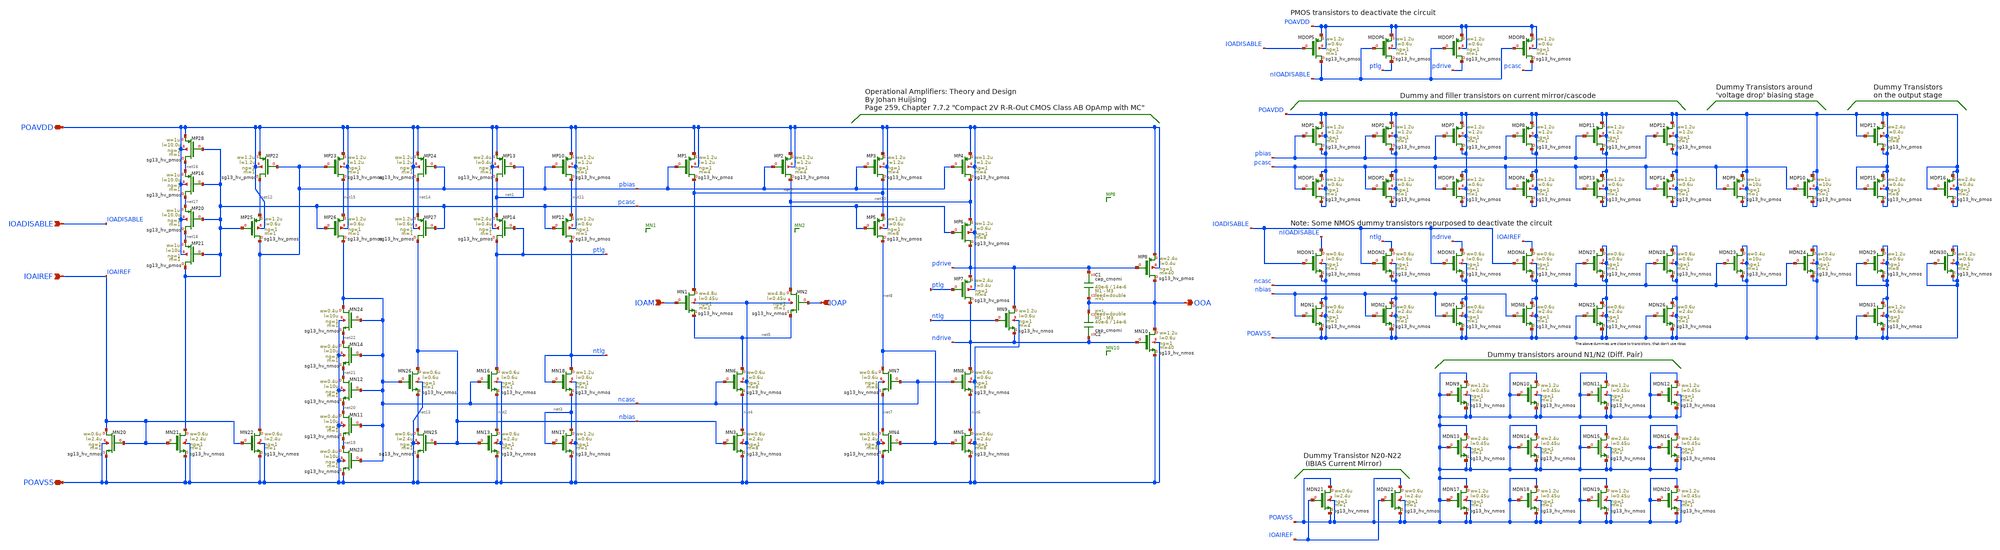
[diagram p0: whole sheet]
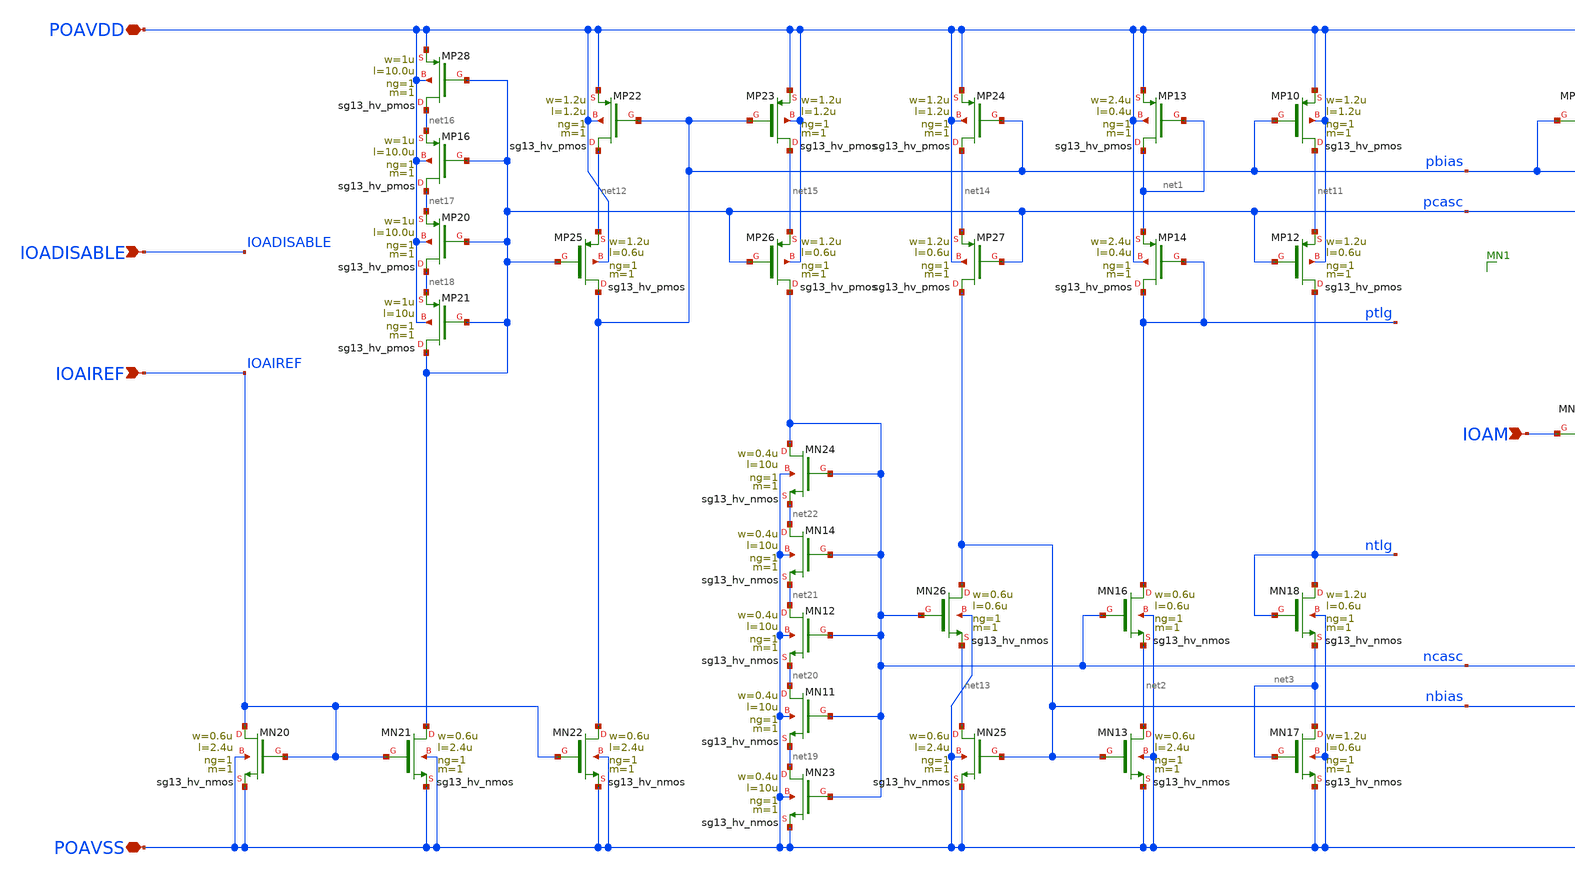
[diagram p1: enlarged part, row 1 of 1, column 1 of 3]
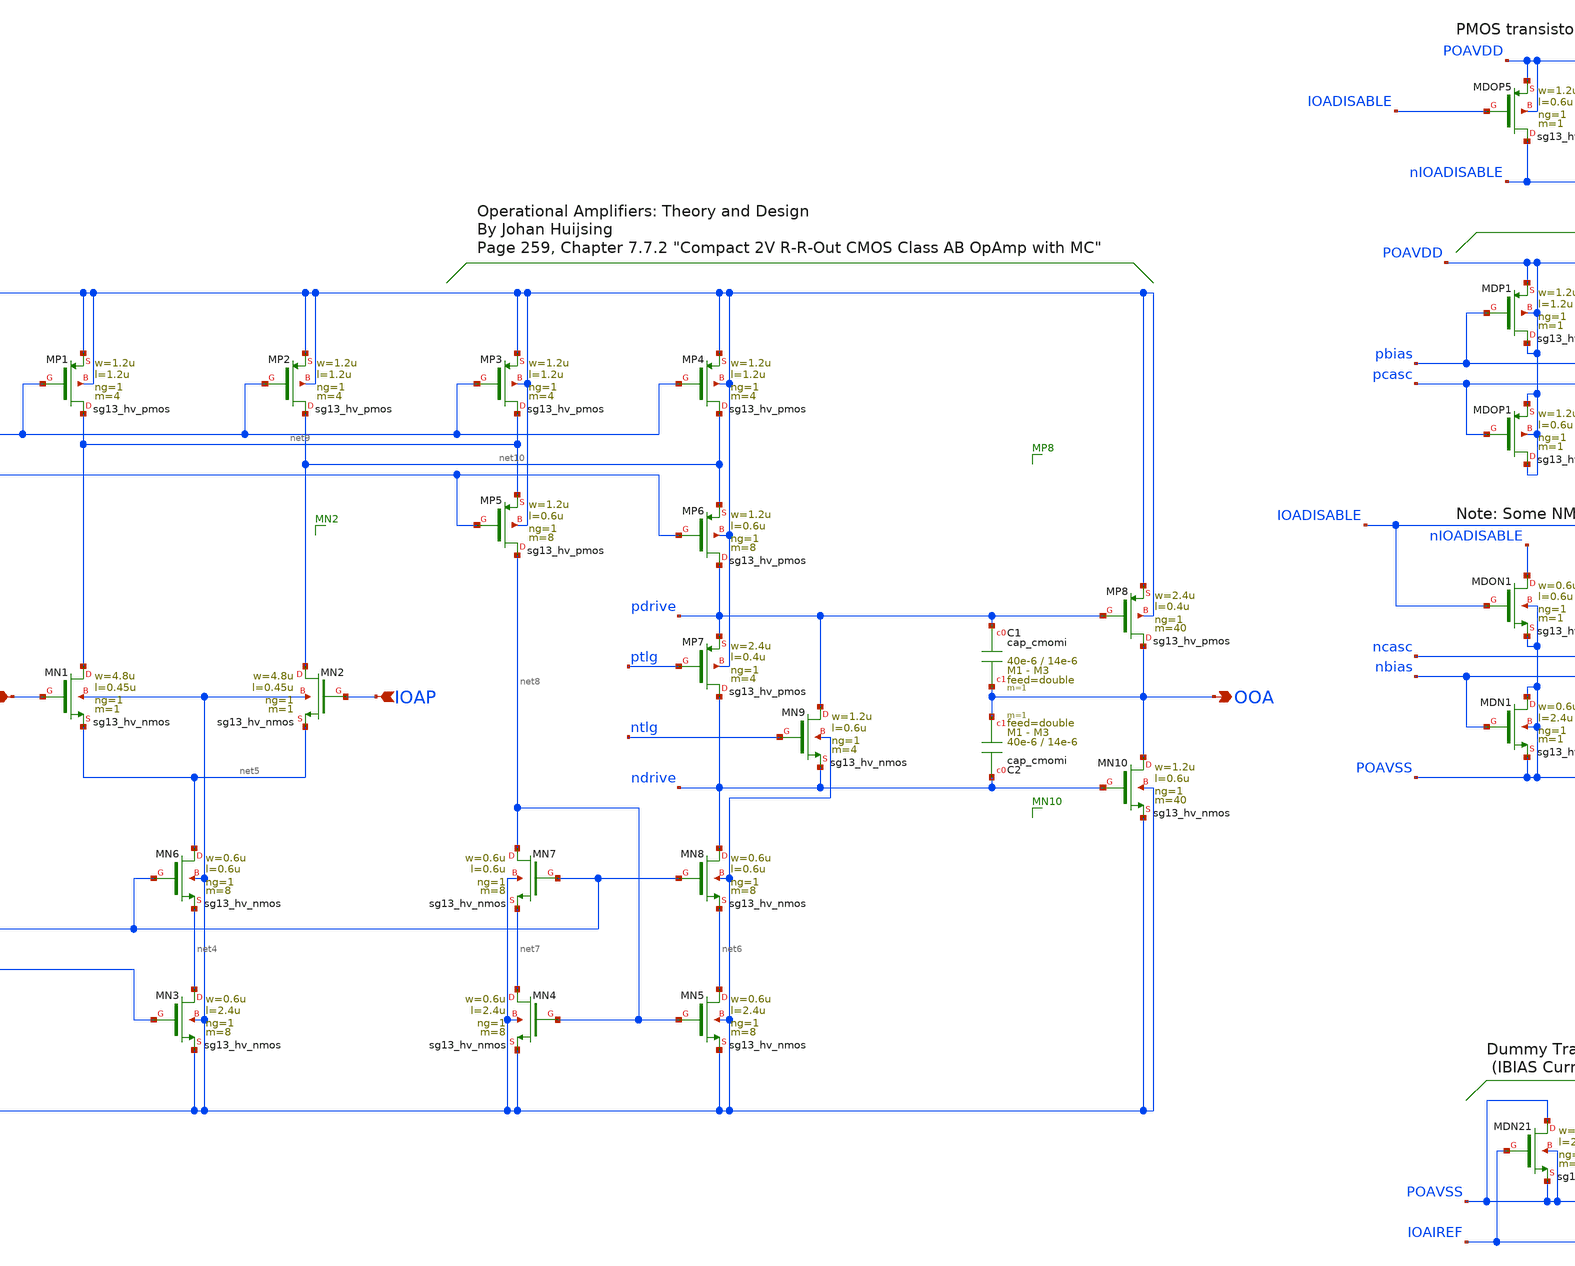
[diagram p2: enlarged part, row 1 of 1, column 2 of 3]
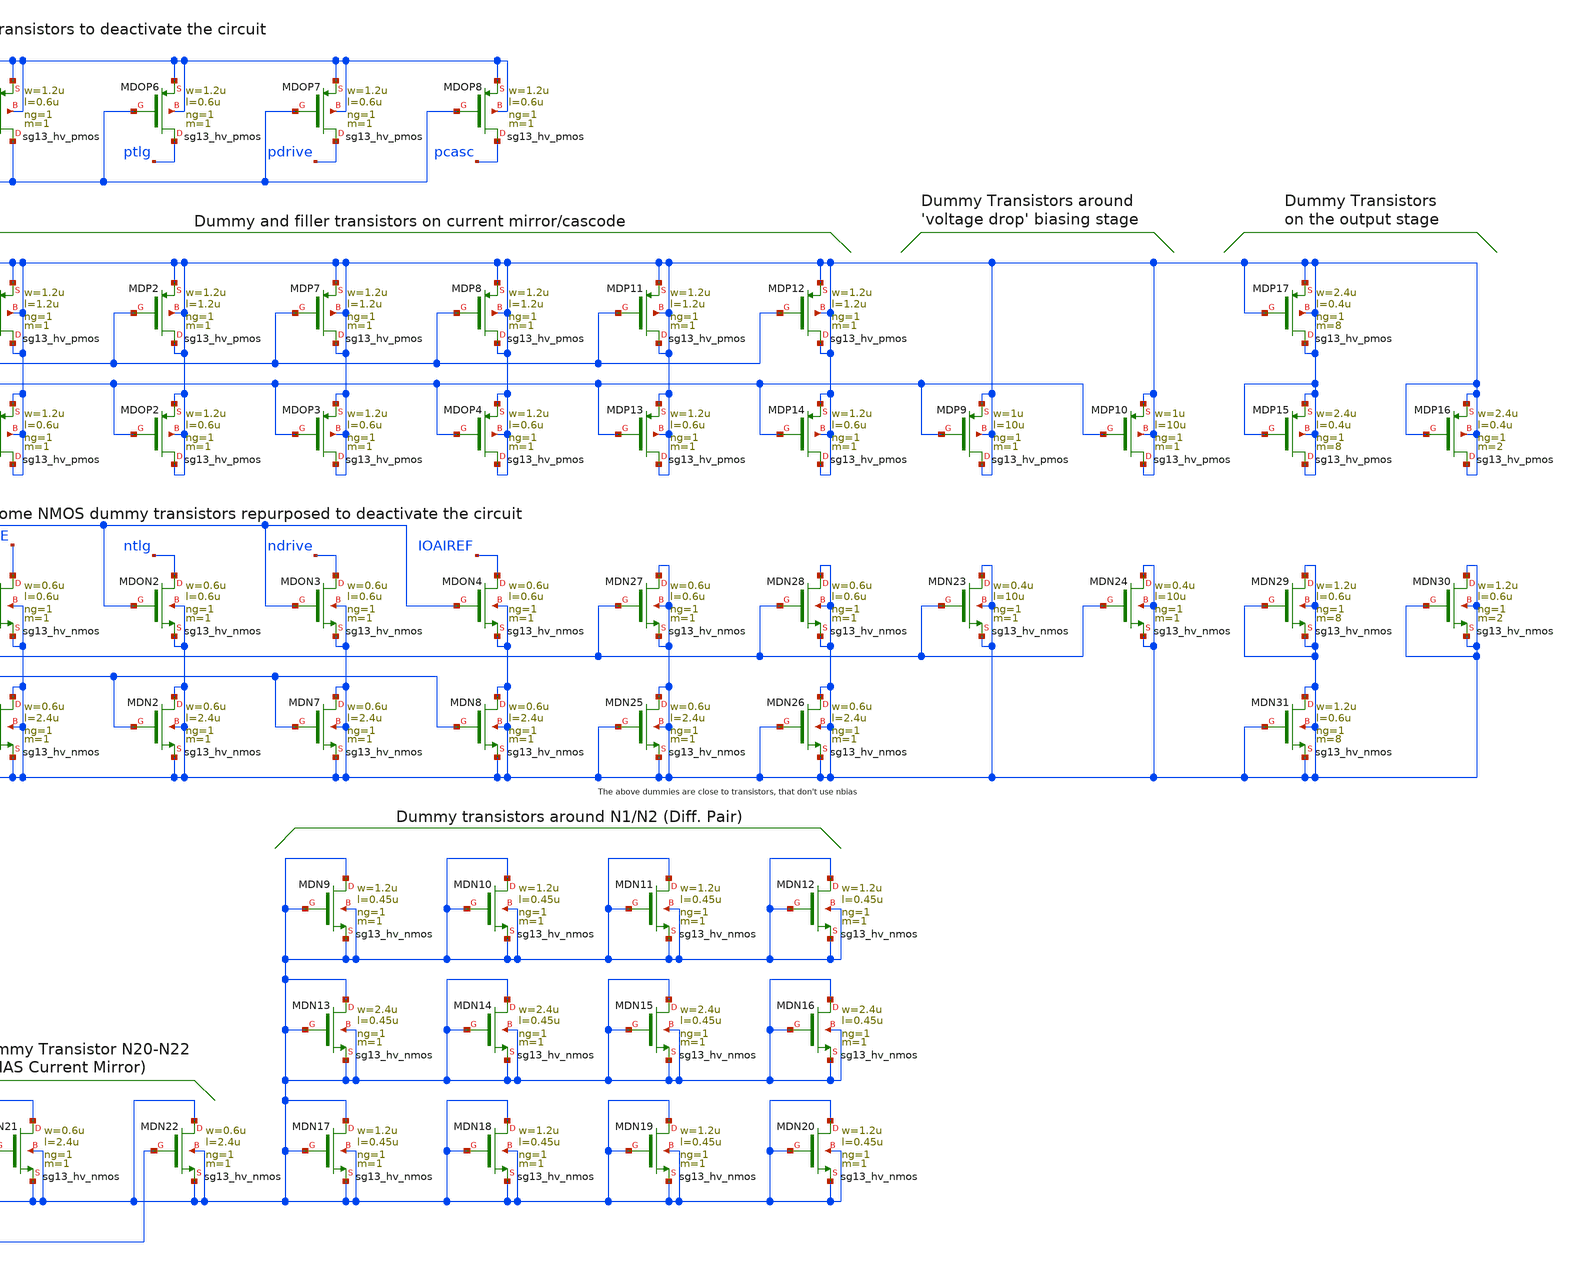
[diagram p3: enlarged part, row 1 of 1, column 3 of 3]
** sch_path: macros/heichips26_FAIf/macros/opamp/schematic/xschem/op_amp_ver_2.sch
**.subckt op_amp_ver_2 POAVDD IOAM IOAP OOA IOAIREF POAVSS IOADISABLE
*.iopin POAVDD
*.ipin IOAM
*.ipin IOAP
*.opin OOA
*.ipin IOAIREF
*.iopin POAVSS
*.ipin IOADISABLE
XMP13 net1 net1 POAVDD POAVDD sg13_hv_pmos w=2.4u l=0.4u ng=1 m=1 mm_ok=1
XMP14 ptlg ptlg net1 POAVDD sg13_hv_pmos w=2.4u l=0.4u ng=1 m=1 mm_ok=1
XMN16 ptlg ncasc net2 POAVSS sg13_hv_nmos w=0.6u l=0.6u ng=1 m=1 mm_ok=1
XMN13 net2 nbias POAVSS POAVSS sg13_hv_nmos w=0.6u l=2.4u ng=1 m=1 mm_ok=1
XMN18 ntlg ntlg net3 POAVSS sg13_hv_nmos w=1.2u l=0.6u ng=1 m=1 mm_ok=1
XMN17 net3 net3 POAVSS POAVSS sg13_hv_nmos w=1.2u l=0.6u ng=1 m=1 mm_ok=1
XMP10 net11 pbias POAVDD POAVDD sg13_hv_pmos w=1.2u l=1.2u ng=1 m=1 mm_ok=1
XMP12 ntlg pcasc net11 POAVDD sg13_hv_pmos w=1.2u l=0.6u ng=1 m=1 mm_ok=1
XMP1 net9 pbias POAVDD POAVDD sg13_hv_pmos w=1.2u l=1.2u ng=1 m=4 mm_ok=1
XMP2 net10 pbias POAVDD POAVDD sg13_hv_pmos w=1.2u l=1.2u ng=1 m=4 mm_ok=1
XMN1 net9 IOAM net5 POAVSS sg13_hv_nmos w=4.8u l=0.45u ng=1 m=1 mm_ok=1
XMN2 net10 IOAP net5 POAVSS sg13_hv_nmos w=4.8u l=0.45u ng=1 m=1 mm_ok=1
XMN3 net4 nbias POAVSS POAVSS sg13_hv_nmos w=0.6u l=2.4u ng=1 m=8 mm_ok=1
XMN6 net5 ncasc net4 POAVSS sg13_hv_nmos w=0.6u l=0.6u ng=1 m=8 mm_ok=1
XMN7 net8 ncasc net7 POAVSS sg13_hv_nmos w=0.6u l=0.6u ng=1 m=8 mm_ok=1
XMN8 ndrive ncasc net6 POAVSS sg13_hv_nmos w=0.6u l=0.6u ng=1 m=8 mm_ok=1
XMN4 net7 net8 POAVSS POAVSS sg13_hv_nmos w=0.6u l=2.4u ng=1 m=8 mm_ok=1
XMN5 net6 net8 POAVSS POAVSS sg13_hv_nmos w=0.6u l=2.4u ng=1 m=8 mm_ok=1
XMP3 net9 pbias POAVDD POAVDD sg13_hv_pmos w=1.2u l=1.2u ng=1 m=4 mm_ok=1
XMP5 net8 pcasc net9 POAVDD sg13_hv_pmos w=1.2u l=0.6u ng=1 m=8 mm_ok=1
XMP4 net10 pbias POAVDD POAVDD sg13_hv_pmos w=1.2u l=1.2u ng=1 m=4 mm_ok=1
XMP6 pdrive pcasc net10 POAVDD sg13_hv_pmos w=1.2u l=0.6u ng=1 m=8 mm_ok=1
XMP7 ndrive ptlg pdrive POAVDD sg13_hv_pmos w=2.4u l=0.4u ng=1 m=4 mm_ok=1
XMN9 pdrive ntlg ndrive POAVSS sg13_hv_nmos w=1.2u l=0.6u ng=1 m=4 mm_ok=1
XMP8 OOA pdrive POAVDD POAVDD sg13_hv_pmos w=2.4u l=0.4u ng=1 m=40 mm_ok=1
XMN10 OOA ndrive POAVSS POAVSS sg13_hv_nmos w=1.2u l=0.6u ng=1 m=40 mm_ok=1
XMN20 IOAIREF IOAIREF POAVSS POAVSS sg13_hv_nmos w=0.6u l=2.4u ng=1 m=1 mm_ok=1
XMN21 pcasc IOAIREF POAVSS POAVSS sg13_hv_nmos w=0.6u l=2.4u ng=1 m=1 mm_ok=1
XMN22 pbias IOAIREF POAVSS POAVSS sg13_hv_nmos w=0.6u l=2.4u ng=1 m=1 mm_ok=1
XMN23 net19 ncasc POAVSS POAVSS sg13_hv_nmos w=0.4u l=10u ng=1 m=1 mm_ok=1
XMN25 net13 nbias POAVSS POAVSS sg13_hv_nmos w=0.6u l=2.4u ng=1 m=1 mm_ok=1
XMN24 ncasc ncasc net22 POAVSS sg13_hv_nmos w=0.4u l=10u ng=1 m=1 mm_ok=1
XMN26 nbias ncasc net13 POAVSS sg13_hv_nmos w=0.6u l=0.6u ng=1 m=1 mm_ok=1
XMP21 pcasc pcasc net18 POAVDD sg13_hv_pmos w=1u l=10u ng=1 m=1 mm_ok=1
XMP20 net18 pcasc net17 POAVDD sg13_hv_pmos w=1u l=10.0u ng=1 m=1 mm_ok=1
XMP22 net12 pbias POAVDD POAVDD sg13_hv_pmos w=1.2u l=1.2u ng=1 m=1 mm_ok=1
XMP25 pbias pcasc net12 POAVDD sg13_hv_pmos w=1.2u l=0.6u ng=1 m=1 mm_ok=1
XMP26 ncasc pcasc net15 POAVDD sg13_hv_pmos w=1.2u l=0.6u ng=1 m=1 mm_ok=1
XMP23 net15 pbias POAVDD POAVDD sg13_hv_pmos w=1.2u l=1.2u ng=1 m=1 mm_ok=1
XMP24 net14 pbias POAVDD POAVDD sg13_hv_pmos w=1.2u l=1.2u ng=1 m=1 mm_ok=1
XMP27 nbias pcasc net14 POAVDD sg13_hv_pmos w=1.2u l=0.6u ng=1 m=1 mm_ok=1
XMP16 net17 pcasc net16 POAVDD sg13_hv_pmos w=1u l=10.0u ng=1 m=1 mm_ok=1
XMN11 net20 ncasc net19 POAVSS sg13_hv_nmos w=0.4u l=10u ng=1 m=1 mm_ok=1
XMP28 net16 pcasc POAVDD POAVDD sg13_hv_pmos w=1u l=10.0u ng=1 m=1 mm_ok=1
XMN12 net21 ncasc net20 POAVSS sg13_hv_nmos w=0.4u l=10u ng=1 m=1 mm_ok=1
XMN14 net22 ncasc net21 POAVSS sg13_hv_nmos w=0.4u l=10u ng=1 m=1 mm_ok=1
XMDP1 POAVDD pbias POAVDD POAVDD sg13_hv_pmos w=1.2u l=1.2u ng=1 m=1 mm_ok=1
XMDP2 POAVDD pbias POAVDD POAVDD sg13_hv_pmos w=1.2u l=1.2u ng=1 m=1 mm_ok=1
XMDOP1 POAVDD pcasc POAVDD POAVDD sg13_hv_pmos w=1.2u l=0.6u ng=1 m=1 mm_ok=1
XMDOP2 POAVDD pcasc POAVDD POAVDD sg13_hv_pmos w=1.2u l=0.6u ng=1 m=1 mm_ok=1
XMDOP3 POAVDD pcasc POAVDD POAVDD sg13_hv_pmos w=1.2u l=0.6u ng=1 m=1 mm_ok=1
XMDOP4 POAVDD pcasc POAVDD POAVDD sg13_hv_pmos w=1.2u l=0.6u ng=1 m=1 mm_ok=1
XMDN1 POAVSS nbias POAVSS POAVSS sg13_hv_nmos w=0.6u l=2.4u ng=1 m=1 mm_ok=1
XMDN2 POAVSS nbias POAVSS POAVSS sg13_hv_nmos w=0.6u l=2.4u ng=1 m=1 mm_ok=1
XMDON1 nIOADISABLE IOADISABLE POAVSS POAVSS sg13_hv_nmos w=0.6u l=0.6u ng=1 m=1 mm_ok=1
XMDON2 ntlg IOADISABLE POAVSS POAVSS sg13_hv_nmos w=0.6u l=0.6u ng=1 m=1 mm_ok=1
XMDON3 ndrive IOADISABLE POAVSS POAVSS sg13_hv_nmos w=0.6u l=0.6u ng=1 m=1 mm_ok=1
XMDON4 IOAIREF IOADISABLE POAVSS POAVSS sg13_hv_nmos w=0.6u l=0.6u ng=1 m=1 mm_ok=1
XMDP7 POAVDD pbias POAVDD POAVDD sg13_hv_pmos w=1.2u l=1.2u ng=1 m=1 mm_ok=1
XMDP8 POAVDD pbias POAVDD POAVDD sg13_hv_pmos w=1.2u l=1.2u ng=1 m=1 mm_ok=1
XMDN7 POAVSS nbias POAVSS POAVSS sg13_hv_nmos w=0.6u l=2.4u ng=1 m=1 mm_ok=1
XMDN8 POAVSS nbias POAVSS POAVSS sg13_hv_nmos w=0.6u l=2.4u ng=1 m=1 mm_ok=1
XMDN9 POAVSS POAVSS POAVSS POAVSS sg13_hv_nmos w=1.2u l=0.45u ng=1 m=1 mm_ok=1
XMDN10 POAVSS POAVSS POAVSS POAVSS sg13_hv_nmos w=1.2u l=0.45u ng=1 m=1 mm_ok=1
XMDN11 POAVSS POAVSS POAVSS POAVSS sg13_hv_nmos w=1.2u l=0.45u ng=1 m=1 mm_ok=1
XMDN12 POAVSS POAVSS POAVSS POAVSS sg13_hv_nmos w=1.2u l=0.45u ng=1 m=1 mm_ok=1
XMDN13 POAVSS POAVSS POAVSS POAVSS sg13_hv_nmos w=2.4u l=0.45u ng=1 m=1 mm_ok=1
XMDN14 POAVSS POAVSS POAVSS POAVSS sg13_hv_nmos w=2.4u l=0.45u ng=1 m=1 mm_ok=1
XMDN15 POAVSS POAVSS POAVSS POAVSS sg13_hv_nmos w=2.4u l=0.45u ng=1 m=1 mm_ok=1
XMDN16 POAVSS POAVSS POAVSS POAVSS sg13_hv_nmos w=2.4u l=0.45u ng=1 m=1 mm_ok=1
XMDN17 POAVSS POAVSS POAVSS POAVSS sg13_hv_nmos w=1.2u l=0.45u ng=1 m=1 mm_ok=1
XMDN18 POAVSS POAVSS POAVSS POAVSS sg13_hv_nmos w=1.2u l=0.45u ng=1 m=1 mm_ok=1
XMDN19 POAVSS POAVSS POAVSS POAVSS sg13_hv_nmos w=1.2u l=0.45u ng=1 m=1 mm_ok=1
XMDN20 POAVSS POAVSS POAVSS POAVSS sg13_hv_nmos w=1.2u l=0.45u ng=1 m=1 mm_ok=1
XMDN21 POAVSS IOAIREF POAVSS POAVSS sg13_hv_nmos w=0.6u l=2.4u ng=1 m=1 mm_ok=1
XMDN22 POAVSS IOAIREF POAVSS POAVSS sg13_hv_nmos w=0.6u l=2.4u ng=1 m=1 mm_ok=1
XMDP9 POAVDD pcasc POAVDD POAVDD sg13_hv_pmos w=1u l=10u ng=1 m=1 mm_ok=1
XMDN23 POAVSS ncasc POAVSS POAVSS sg13_hv_nmos w=0.4u l=10u ng=1 m=1 mm_ok=1
XMDP10 POAVDD pcasc POAVDD POAVDD sg13_hv_pmos w=1u l=10u ng=1 m=1 mm_ok=1
XMDN24 POAVSS ncasc POAVSS POAVSS sg13_hv_nmos w=0.4u l=10u ng=1 m=1 mm_ok=1
XMDP11 POAVDD pbias POAVDD POAVDD sg13_hv_pmos w=1.2u l=1.2u ng=1 m=1 mm_ok=1
XMDP12 POAVDD pbias POAVDD POAVDD sg13_hv_pmos w=1.2u l=1.2u ng=1 m=1 mm_ok=1
XMDP13 POAVDD pcasc POAVDD POAVDD sg13_hv_pmos w=1.2u l=0.6u ng=1 m=1 mm_ok=1
XMDP14 POAVDD pcasc POAVDD POAVDD sg13_hv_pmos w=1.2u l=0.6u ng=1 m=1 mm_ok=1
XMDN25 POAVSS POAVSS POAVSS POAVSS sg13_hv_nmos w=0.6u l=2.4u ng=1 m=1 mm_ok=1
XMDN26 POAVSS POAVSS POAVSS POAVSS sg13_hv_nmos w=0.6u l=2.4u ng=1 m=1 mm_ok=1
XMDN27 POAVSS ncasc POAVSS POAVSS sg13_hv_nmos w=0.6u l=0.6u ng=1 m=1 mm_ok=1
XMDN28 POAVSS ncasc POAVSS POAVSS sg13_hv_nmos w=0.6u l=0.6u ng=1 m=1 mm_ok=1
XMDP15 POAVDD POAVDD POAVDD POAVDD sg13_hv_pmos w=2.4u l=0.4u ng=1 m=8 mm_ok=1
XMDN29 POAVSS POAVSS POAVSS POAVSS sg13_hv_nmos w=1.2u l=0.6u ng=1 m=8 mm_ok=1
XMDP16 POAVDD POAVDD POAVDD POAVDD sg13_hv_pmos w=2.4u l=0.4u ng=1 m=2 mm_ok=1
XMDN30 POAVSS POAVSS POAVSS POAVSS sg13_hv_nmos w=1.2u l=0.6u ng=1 m=2 mm_ok=1
XMDP17 POAVDD POAVDD POAVDD POAVDD sg13_hv_pmos w=2.4u l=0.4u ng=1 m=8 mm_ok=1
XMDN31 POAVSS POAVSS POAVSS POAVSS sg13_hv_nmos w=1.2u l=0.6u ng=1 m=8 mm_ok=1
XMDOP5 nIOADISABLE IOADISABLE POAVDD POAVDD sg13_hv_pmos w=1.2u l=0.6u ng=1 m=1 mm_ok=1
XMDOP6 ptlg nIOADISABLE POAVDD POAVDD sg13_hv_pmos w=1.2u l=0.6u ng=1 m=1 mm_ok=1
XMDOP7 pdrive nIOADISABLE POAVDD POAVDD sg13_hv_pmos w=1.2u l=0.6u ng=1 m=1 mm_ok=1
XMDOP8 pcasc nIOADISABLE POAVDD POAVDD sg13_hv_pmos w=1.2u l=0.6u ng=1 m=1 mm_ok=1
XC1 pdrive OOA cap_cmomi w=40e-6 l=14e-6 mmin=1 mmax=3 feed=double subblock=0 m=1 mm_ok=1
XC2 ndrive OOA cap_cmomi w=40e-6 l=14e-6 mmin=1 mmax=3 feed=double subblock=0 m=1 mm_ok=1
**.ends
.end
